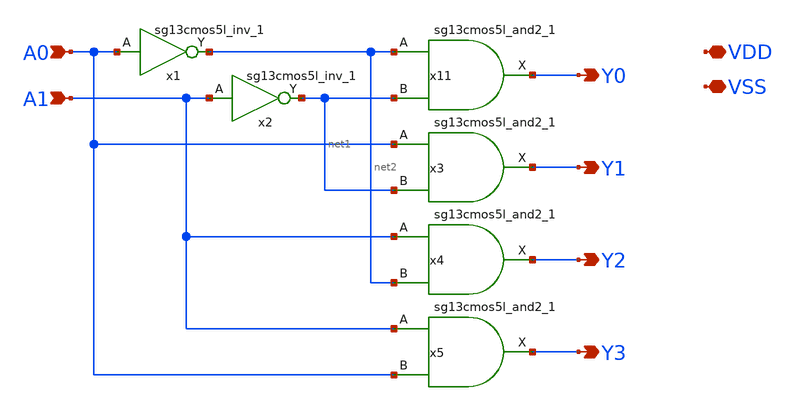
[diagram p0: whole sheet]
** sch_path: designs/libs/core_digital/dec2to4/dec2to4.sch
**.subckt dec2to4 A0 A1 Y0 Y1 Y2 Y3 VDD VSS
*.ipin A0
*.ipin A1
*.opin Y0
*.opin Y1
*.opin Y2
*.opin Y3
*.iopin VDD
*.iopin VSS
x1 net2 A0 VDD VSS sg13cmos5l_inv_1
x2 net1 A1 VDD VSS sg13cmos5l_inv_1
x11 Y0 net2 net1 VDD VSS sg13cmos5l_and2_1
x3 Y1 A0 net1 VDD VSS sg13cmos5l_and2_1
x4 Y2 A1 net2 VDD VSS sg13cmos5l_and2_1
x5 Y3 A1 A0 VDD VSS sg13cmos5l_and2_1
**.ends
.end
